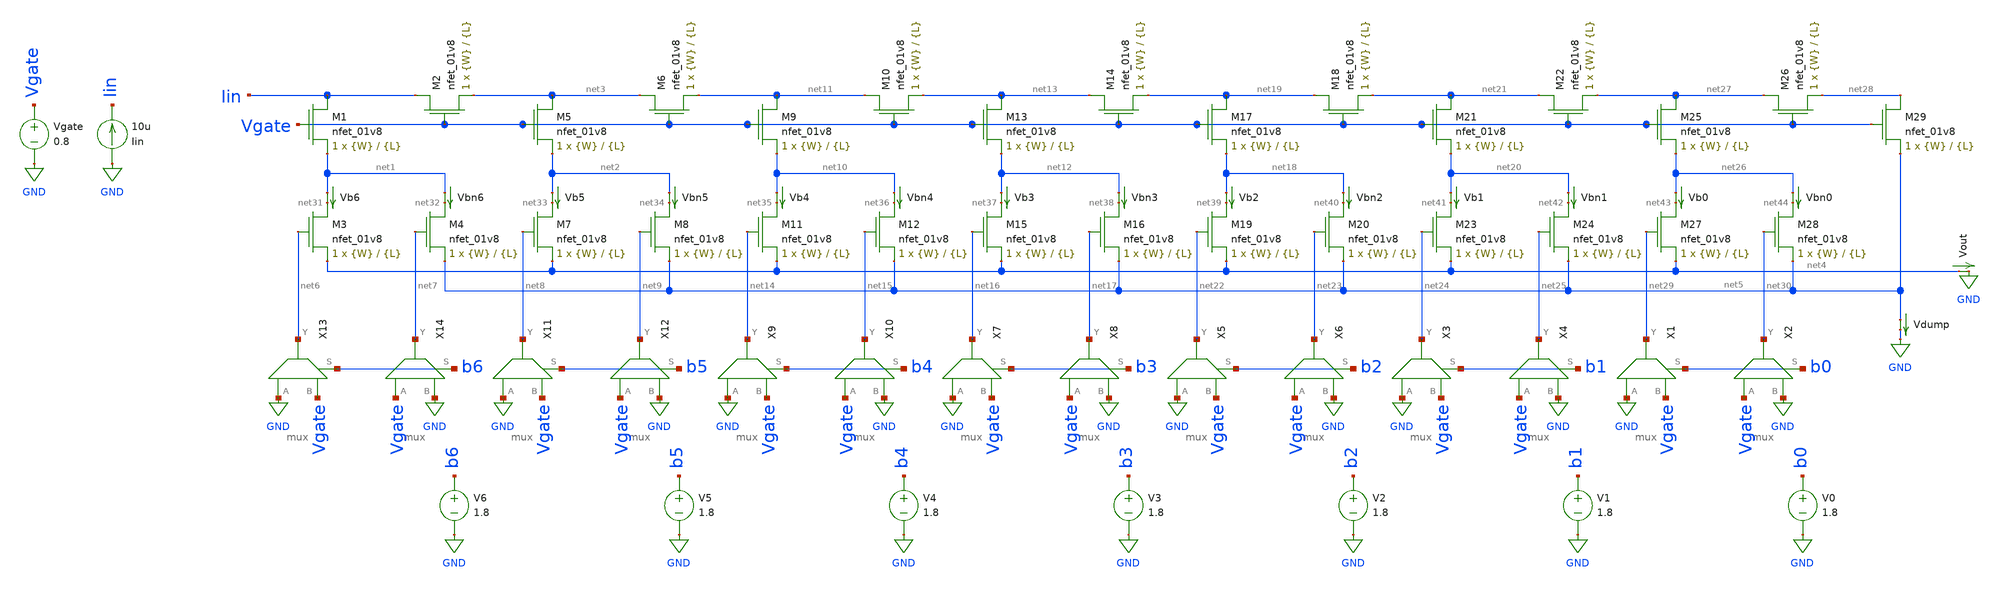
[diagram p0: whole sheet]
** sch_path: schematics/dac_from_paper.sch
**.subckt dac_from_paper
XM1 Iin Vgate net1 GND sky130_fd_pr__nfet_01v8 L={L} W={W} nf=1 ad='int((nf+1)/2) * W/nf * 0.29' as='int((nf+2)/2) * W/nf * 0.29'
+ pd='2*int((nf+1)/2) * (W/nf + 0.29)' ps='2*int((nf+2)/2) * (W/nf + 0.29)' nrd='0.29 / W' nrs='0.29 / W'
+ sa=0 sb=0 sd=0 mult=1 m=1
XM2 Iin Vgate net3 GND sky130_fd_pr__nfet_01v8 L={L} W={W} nf=1 ad='int((nf+1)/2) * W/nf * 0.29' as='int((nf+2)/2) * W/nf * 0.29'
+ pd='2*int((nf+1)/2) * (W/nf + 0.29)' ps='2*int((nf+2)/2) * (W/nf + 0.29)' nrd='0.29 / W' nrs='0.29 / W'
+ sa=0 sb=0 sd=0 mult=1 m=1
XM3 net31 net6 net4 GND sky130_fd_pr__nfet_01v8 L={L} W={W} nf=1 ad='int((nf+1)/2) * W/nf * 0.29' as='int((nf+2)/2) * W/nf * 0.29'
+ pd='2*int((nf+1)/2) * (W/nf + 0.29)' ps='2*int((nf+2)/2) * (W/nf + 0.29)' nrd='0.29 / W' nrs='0.29 / W'
+ sa=0 sb=0 sd=0 mult=1 m=1
XM4 net32 net7 net5 GND sky130_fd_pr__nfet_01v8 L={L} W={W} nf=1 ad='int((nf+1)/2) * W/nf * 0.29' as='int((nf+2)/2) * W/nf * 0.29'
+ pd='2*int((nf+1)/2) * (W/nf + 0.29)' ps='2*int((nf+2)/2) * (W/nf + 0.29)' nrd='0.29 / W' nrs='0.29 / W'
+ sa=0 sb=0 sd=0 mult=1 m=1
XM5 net3 Vgate net2 GND sky130_fd_pr__nfet_01v8 L={L} W={W} nf=1 ad='int((nf+1)/2) * W/nf * 0.29' as='int((nf+2)/2) * W/nf * 0.29'
+ pd='2*int((nf+1)/2) * (W/nf + 0.29)' ps='2*int((nf+2)/2) * (W/nf + 0.29)' nrd='0.29 / W' nrs='0.29 / W'
+ sa=0 sb=0 sd=0 mult=1 m=1
XM6 net3 Vgate net11 GND sky130_fd_pr__nfet_01v8 L={L} W={W} nf=1 ad='int((nf+1)/2) * W/nf * 0.29' as='int((nf+2)/2) * W/nf * 0.29'
+ pd='2*int((nf+1)/2) * (W/nf + 0.29)' ps='2*int((nf+2)/2) * (W/nf + 0.29)' nrd='0.29 / W' nrs='0.29 / W'
+ sa=0 sb=0 sd=0 mult=1 m=1
XM7 net33 net8 net4 GND sky130_fd_pr__nfet_01v8 L={L} W={W} nf=1 ad='int((nf+1)/2) * W/nf * 0.29' as='int((nf+2)/2) * W/nf * 0.29'
+ pd='2*int((nf+1)/2) * (W/nf + 0.29)' ps='2*int((nf+2)/2) * (W/nf + 0.29)' nrd='0.29 / W' nrs='0.29 / W'
+ sa=0 sb=0 sd=0 mult=1 m=1
XM8 net34 net9 net5 GND sky130_fd_pr__nfet_01v8 L={L} W={W} nf=1 ad='int((nf+1)/2) * W/nf * 0.29' as='int((nf+2)/2) * W/nf * 0.29'
+ pd='2*int((nf+1)/2) * (W/nf + 0.29)' ps='2*int((nf+2)/2) * (W/nf + 0.29)' nrd='0.29 / W' nrs='0.29 / W'
+ sa=0 sb=0 sd=0 mult=1 m=1
XM9 net11 Vgate net10 GND sky130_fd_pr__nfet_01v8 L={L} W={W} nf=1 ad='int((nf+1)/2) * W/nf * 0.29' as='int((nf+2)/2) * W/nf * 0.29'
+ pd='2*int((nf+1)/2) * (W/nf + 0.29)' ps='2*int((nf+2)/2) * (W/nf + 0.29)' nrd='0.29 / W' nrs='0.29 / W'
+ sa=0 sb=0 sd=0 mult=1 m=1
XM10 net11 Vgate net13 GND sky130_fd_pr__nfet_01v8 L={L} W={W} nf=1 ad='int((nf+1)/2) * W/nf * 0.29'
+ as='int((nf+2)/2) * W/nf * 0.29' pd='2*int((nf+1)/2) * (W/nf + 0.29)' ps='2*int((nf+2)/2) * (W/nf + 0.29)'
+ nrd='0.29 / W' nrs='0.29 / W' sa=0 sb=0 sd=0 mult=1 m=1
XM11 net35 net14 net4 GND sky130_fd_pr__nfet_01v8 L={L} W={W} nf=1 ad='int((nf+1)/2) * W/nf * 0.29' as='int((nf+2)/2) * W/nf * 0.29'
+ pd='2*int((nf+1)/2) * (W/nf + 0.29)' ps='2*int((nf+2)/2) * (W/nf + 0.29)' nrd='0.29 / W' nrs='0.29 / W'
+ sa=0 sb=0 sd=0 mult=1 m=1
XM12 net36 net15 net5 GND sky130_fd_pr__nfet_01v8 L={L} W={W} nf=1 ad='int((nf+1)/2) * W/nf * 0.29' as='int((nf+2)/2) * W/nf * 0.29'
+ pd='2*int((nf+1)/2) * (W/nf + 0.29)' ps='2*int((nf+2)/2) * (W/nf + 0.29)' nrd='0.29 / W' nrs='0.29 / W'
+ sa=0 sb=0 sd=0 mult=1 m=1
XM13 net13 Vgate net12 GND sky130_fd_pr__nfet_01v8 L={L} W={W} nf=1 ad='int((nf+1)/2) * W/nf * 0.29'
+ as='int((nf+2)/2) * W/nf * 0.29' pd='2*int((nf+1)/2) * (W/nf + 0.29)' ps='2*int((nf+2)/2) * (W/nf + 0.29)'
+ nrd='0.29 / W' nrs='0.29 / W' sa=0 sb=0 sd=0 mult=1 m=1
XM14 net13 Vgate net19 GND sky130_fd_pr__nfet_01v8 L={L} W={W} nf=1 ad='int((nf+1)/2) * W/nf * 0.29'
+ as='int((nf+2)/2) * W/nf * 0.29' pd='2*int((nf+1)/2) * (W/nf + 0.29)' ps='2*int((nf+2)/2) * (W/nf + 0.29)'
+ nrd='0.29 / W' nrs='0.29 / W' sa=0 sb=0 sd=0 mult=1 m=1
XM15 net37 net16 net4 GND sky130_fd_pr__nfet_01v8 L={L} W={W} nf=1 ad='int((nf+1)/2) * W/nf * 0.29' as='int((nf+2)/2) * W/nf * 0.29'
+ pd='2*int((nf+1)/2) * (W/nf + 0.29)' ps='2*int((nf+2)/2) * (W/nf + 0.29)' nrd='0.29 / W' nrs='0.29 / W'
+ sa=0 sb=0 sd=0 mult=1 m=1
XM16 net38 net17 net5 GND sky130_fd_pr__nfet_01v8 L={L} W={W} nf=1 ad='int((nf+1)/2) * W/nf * 0.29' as='int((nf+2)/2) * W/nf * 0.29'
+ pd='2*int((nf+1)/2) * (W/nf + 0.29)' ps='2*int((nf+2)/2) * (W/nf + 0.29)' nrd='0.29 / W' nrs='0.29 / W'
+ sa=0 sb=0 sd=0 mult=1 m=1
XM17 net19 Vgate net18 GND sky130_fd_pr__nfet_01v8 L={L} W={W} nf=1 ad='int((nf+1)/2) * W/nf * 0.29'
+ as='int((nf+2)/2) * W/nf * 0.29' pd='2*int((nf+1)/2) * (W/nf + 0.29)' ps='2*int((nf+2)/2) * (W/nf + 0.29)'
+ nrd='0.29 / W' nrs='0.29 / W' sa=0 sb=0 sd=0 mult=1 m=1
XM18 net19 Vgate net21 GND sky130_fd_pr__nfet_01v8 L={L} W={W} nf=1 ad='int((nf+1)/2) * W/nf * 0.29'
+ as='int((nf+2)/2) * W/nf * 0.29' pd='2*int((nf+1)/2) * (W/nf + 0.29)' ps='2*int((nf+2)/2) * (W/nf + 0.29)'
+ nrd='0.29 / W' nrs='0.29 / W' sa=0 sb=0 sd=0 mult=1 m=1
XM19 net39 net22 net4 GND sky130_fd_pr__nfet_01v8 L={L} W={W} nf=1 ad='int((nf+1)/2) * W/nf * 0.29' as='int((nf+2)/2) * W/nf * 0.29'
+ pd='2*int((nf+1)/2) * (W/nf + 0.29)' ps='2*int((nf+2)/2) * (W/nf + 0.29)' nrd='0.29 / W' nrs='0.29 / W'
+ sa=0 sb=0 sd=0 mult=1 m=1
XM20 net40 net23 net5 GND sky130_fd_pr__nfet_01v8 L={L} W={W} nf=1 ad='int((nf+1)/2) * W/nf * 0.29' as='int((nf+2)/2) * W/nf * 0.29'
+ pd='2*int((nf+1)/2) * (W/nf + 0.29)' ps='2*int((nf+2)/2) * (W/nf + 0.29)' nrd='0.29 / W' nrs='0.29 / W'
+ sa=0 sb=0 sd=0 mult=1 m=1
XM21 net21 Vgate net20 GND sky130_fd_pr__nfet_01v8 L={L} W={W} nf=1 ad='int((nf+1)/2) * W/nf * 0.29'
+ as='int((nf+2)/2) * W/nf * 0.29' pd='2*int((nf+1)/2) * (W/nf + 0.29)' ps='2*int((nf+2)/2) * (W/nf + 0.29)'
+ nrd='0.29 / W' nrs='0.29 / W' sa=0 sb=0 sd=0 mult=1 m=1
XM22 net21 Vgate net27 GND sky130_fd_pr__nfet_01v8 L={L} W={W} nf=1 ad='int((nf+1)/2) * W/nf * 0.29'
+ as='int((nf+2)/2) * W/nf * 0.29' pd='2*int((nf+1)/2) * (W/nf + 0.29)' ps='2*int((nf+2)/2) * (W/nf + 0.29)'
+ nrd='0.29 / W' nrs='0.29 / W' sa=0 sb=0 sd=0 mult=1 m=1
XM23 net41 net24 net4 GND sky130_fd_pr__nfet_01v8 L={L} W={W} nf=1 ad='int((nf+1)/2) * W/nf * 0.29' as='int((nf+2)/2) * W/nf * 0.29'
+ pd='2*int((nf+1)/2) * (W/nf + 0.29)' ps='2*int((nf+2)/2) * (W/nf + 0.29)' nrd='0.29 / W' nrs='0.29 / W'
+ sa=0 sb=0 sd=0 mult=1 m=1
XM24 net42 net25 net5 GND sky130_fd_pr__nfet_01v8 L={L} W={W} nf=1 ad='int((nf+1)/2) * W/nf * 0.29' as='int((nf+2)/2) * W/nf * 0.29'
+ pd='2*int((nf+1)/2) * (W/nf + 0.29)' ps='2*int((nf+2)/2) * (W/nf + 0.29)' nrd='0.29 / W' nrs='0.29 / W'
+ sa=0 sb=0 sd=0 mult=1 m=1
XM25 net27 Vgate net26 GND sky130_fd_pr__nfet_01v8 L={L} W={W} nf=1 ad='int((nf+1)/2) * W/nf * 0.29'
+ as='int((nf+2)/2) * W/nf * 0.29' pd='2*int((nf+1)/2) * (W/nf + 0.29)' ps='2*int((nf+2)/2) * (W/nf + 0.29)'
+ nrd='0.29 / W' nrs='0.29 / W' sa=0 sb=0 sd=0 mult=1 m=1
XM26 net27 Vgate net28 GND sky130_fd_pr__nfet_01v8 L={L} W={W} nf=1 ad='int((nf+1)/2) * W/nf * 0.29'
+ as='int((nf+2)/2) * W/nf * 0.29' pd='2*int((nf+1)/2) * (W/nf + 0.29)' ps='2*int((nf+2)/2) * (W/nf + 0.29)'
+ nrd='0.29 / W' nrs='0.29 / W' sa=0 sb=0 sd=0 mult=1 m=1
XM27 net43 net29 net4 GND sky130_fd_pr__nfet_01v8 L={L} W={W} nf=1 ad='int((nf+1)/2) * W/nf * 0.29' as='int((nf+2)/2) * W/nf * 0.29'
+ pd='2*int((nf+1)/2) * (W/nf + 0.29)' ps='2*int((nf+2)/2) * (W/nf + 0.29)' nrd='0.29 / W' nrs='0.29 / W'
+ sa=0 sb=0 sd=0 mult=1 m=1
XM28 net44 net30 net5 GND sky130_fd_pr__nfet_01v8 L={L} W={W} nf=1 ad='int((nf+1)/2) * W/nf * 0.29' as='int((nf+2)/2) * W/nf * 0.29'
+ pd='2*int((nf+1)/2) * (W/nf + 0.29)' ps='2*int((nf+2)/2) * (W/nf + 0.29)' nrd='0.29 / W' nrs='0.29 / W'
+ sa=0 sb=0 sd=0 mult=1 m=1
XM29 net28 Vgate net5 GND sky130_fd_pr__nfet_01v8 L={L} W={W} nf=1 ad='int((nf+1)/2) * W/nf * 0.29' as='int((nf+2)/2) * W/nf * 0.29'
+ pd='2*int((nf+1)/2) * (W/nf + 0.29)' ps='2*int((nf+2)/2) * (W/nf + 0.29)' nrd='0.29 / W' nrs='0.29 / W'
+ sa=0 sb=0 sd=0 mult=1 m=1
Vdump net5 GND 0
.save i(vdump)
Vgate Vgate GND 0.8
Vb0 net26 net43 0
.save i(vb0)
Vbn0 net26 net44 0
.save i(vbn0)
Vb5 net2 net33 0
.save i(vb5)
Vb6 net1 net31 0
.save i(vb6)
Iin GND Iin 10u
Vout net4 GND 0
.save i(vout)
Vb1 net20 net41 0
.save i(vb1)
Vb2 net18 net39 0
.save i(vb2)
Vb3 net12 net37 0
.save i(vb3)
Vb4 net10 net35 0
.save i(vb4)
Vbn1 net20 net42 0
.save i(vbn1)
Vbn2 net18 net40 0
.save i(vbn2)
Vbn3 net12 net38 0
.save i(vbn3)
Vbn4 net10 net36 0
.save i(vbn4)
Vbn5 net2 net34 0
.save i(vbn5)
Vbn6 net1 net32 0
.save i(vbn6)
X1 GND Vgate net29 b0 mux
X2 Vgate GND net30 b0 mux
V0 b0 GND 1.8
X3 GND Vgate net24 b1 mux
X4 Vgate GND net25 b1 mux
V1 b1 GND 1.8
X5 GND Vgate net22 b2 mux
X6 Vgate GND net23 b2 mux
V2 b2 GND 1.8
X7 GND Vgate net16 b3 mux
X8 Vgate GND net17 b3 mux
V3 b3 GND 1.8
X9 GND Vgate net14 b4 mux
X10 Vgate GND net15 b4 mux
V4 b4 GND 1.8
X11 GND Vgate net8 b5 mux
X12 Vgate GND net9 b5 mux
V5 b5 GND 1.8
X13 GND Vgate net6 b6 mux
X14 Vgate GND net7 b6 mux
V6 b6 GND 1.8
**** begin user architecture code

.option wnflag=1
.param MC_SWITCH=0.0
.lib ~/skywater/skywater-pdk/libraries/sky130_fd_pr_ngspice/latest/models/sky130.lib.spice tt


.param W=1
.param L=8
.control
set wr_vecnames
set wr_singlescale
let code = 0
  while code < 128
    if code eq 0
      let b0 = 0
    else
      let b0 = code % 2
    end
    if floor(code / 2) eq 0
      let b1 = 0
    else
      let b1 = floor(code / 2) % 2
    end
    if floor(code / 4) eq 0
      let b2 = 0
    else
      let b2 = floor(code / 4) % 2
    end
    if floor(code / 8) eq 0
      let b3 = 0
    else
      let b3 = floor(code / 8) % 2
    end
    if floor(code / 16) eq 0
      let b4 = 0
    else
      let b4 = floor(code / 16) % 2
    end
    if floor(code / 32) eq 0
      let b5 = 0
    else
      let b5 = floor(code / 32) % 2
    end
    if floor(code / 64) eq 0
      let b6 = 0
    else
      let b6 = floor(code / 64) % 2
    end
    alter vb0 $&b0
    alter vb1 $&b1
    alter vb2 $&b2
    alter vb3 $&b3
    alter vb4 $&b4
    alter vb5 $&b5
    alter vb6 $&b6
    save all
    op
    wrdata ~/Documents/current-output-dac-vlsi/simulations/dac_paper_sim.txt i(vb0) i(vb1) i(vb2)
+ i(vb3) i(vb4) i(vb5) i(vb6) i(Vout) i(Vdump)
    if code eq 0
      set appendwrite
      set wr_vecnames = FALSE
    end
    let code = code + 1
  end
  quit
.endc

**** end user architecture code
**.ends

* expanding   symbol:  /home/madvlsi/Documents/current-output-dac-vlsi/schematics/mux.sym # of
*+ pins=4
** sym_path: /home/madvlsi/Documents/current-output-dac-vlsi/schematics/mux.sym
** sch_path: /home/madvlsi/Documents/current-output-dac-vlsi/schematics/mux.sch
.subckt mux A B Y S
*.ipin S
*.ipin A
*.opin Y
*.ipin B
XM1 net1 S GND GND sky130_fd_pr__nfet_01v8 L=0.15 W=1 nf=1 ad='int((nf+1)/2) * W/nf * 0.29' as='int((nf+2)/2) * W/nf * 0.29'
+ pd='2*int((nf+1)/2) * (W/nf + 0.29)' ps='2*int((nf+2)/2) * (W/nf + 0.29)' nrd='0.29 / W' nrs='0.29 / W'
+ sa=0 sb=0 sd=0 mult=1 m=1
XM2 net1 S VDD VDD sky130_fd_pr__pfet_01v8 L=0.15 W=1 nf=1 ad='int((nf+1)/2) * W/nf * 0.29' as='int((nf+2)/2) * W/nf * 0.29'
+ pd='2*int((nf+1)/2) * (W/nf + 0.29)' ps='2*int((nf+2)/2) * (W/nf + 0.29)' nrd='0.29 / W' nrs='0.29 / W'
+ sa=0 sb=0 sd=0 mult=1 m=1
XM3 Y S B GND sky130_fd_pr__nfet_01v8 L=0.15 W=1 nf=1 ad='int((nf+1)/2) * W/nf * 0.29' as='int((nf+2)/2) * W/nf * 0.29'
+ pd='2*int((nf+1)/2) * (W/nf + 0.29)' ps='2*int((nf+2)/2) * (W/nf + 0.29)' nrd='0.29 / W' nrs='0.29 / W'
+ sa=0 sb=0 sd=0 mult=1 m=1
XM4 A net1 Y GND sky130_fd_pr__nfet_01v8 L=0.15 W=1 nf=1 ad='int((nf+1)/2) * W/nf * 0.29' as='int((nf+2)/2) * W/nf * 0.29'
+ pd='2*int((nf+1)/2) * (W/nf + 0.29)' ps='2*int((nf+2)/2) * (W/nf + 0.29)' nrd='0.29 / W' nrs='0.29 / W'
+ sa=0 sb=0 sd=0 mult=1 m=1
.ends

.GLOBAL GND
.GLOBAL VDD
.end
